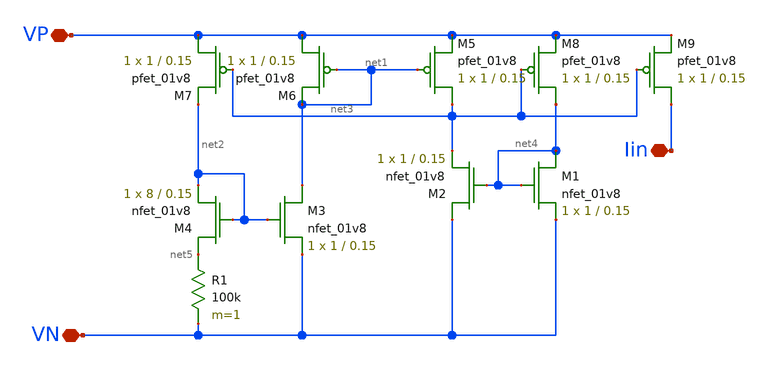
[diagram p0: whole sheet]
** sch_path: biasGen.sch
**.subckt biasGen VN Iin VP
*.iopin VN
*.iopin Iin
*.iopin VP
XM1 net4 net4 VN GND sky130_fd_pr__nfet_01v8 L=0.15 W=1 nf=1 ad='int((nf+1)/2) * W/nf * 0.29' as='int((nf+2)/2) * W/nf * 0.29'
+ pd='2*int((nf+1)/2) * (W/nf + 0.29)' ps='2*int((nf+2)/2) * (W/nf + 0.29)' nrd='0.29 / W' nrs='0.29 / W'
+ sa=0 sb=0 sd=0 mult=1 m=1
XM2 VN net4 net3 GND sky130_fd_pr__nfet_01v8 L=0.15 W=1 nf=1 ad='int((nf+1)/2) * W/nf * 0.29' as='int((nf+2)/2) * W/nf * 0.29'
+ pd='2*int((nf+1)/2) * (W/nf + 0.29)' ps='2*int((nf+2)/2) * (W/nf + 0.29)' nrd='0.29 / W' nrs='0.29 / W'
+ sa=0 sb=0 sd=0 mult=1 m=1
XM3 net1 net2 VN GND sky130_fd_pr__nfet_01v8 L=0.15 W=1 nf=1 ad='int((nf+1)/2) * W/nf * 0.29' as='int((nf+2)/2) * W/nf * 0.29'
+ pd='2*int((nf+1)/2) * (W/nf + 0.29)' ps='2*int((nf+2)/2) * (W/nf + 0.29)' nrd='0.29 / W' nrs='0.29 / W'
+ sa=0 sb=0 sd=0 mult=1 m=1
XM4 net5 net2 net2 GND sky130_fd_pr__nfet_01v8 L=0.15 W=8 nf=1 ad='int((nf+1)/2) * W/nf * 0.29' as='int((nf+2)/2) * W/nf * 0.29'
+ pd='2*int((nf+1)/2) * (W/nf + 0.29)' ps='2*int((nf+2)/2) * (W/nf + 0.29)' nrd='0.29 / W' nrs='0.29 / W'
+ sa=0 sb=0 sd=0 mult=1 m=1
XM5 net3 net1 VP VDD sky130_fd_pr__pfet_01v8 L=0.15 W=1 nf=1 ad='int((nf+1)/2) * W/nf * 0.29' as='int((nf+2)/2) * W/nf * 0.29'
+ pd='2*int((nf+1)/2) * (W/nf + 0.29)' ps='2*int((nf+2)/2) * (W/nf + 0.29)' nrd='0.29 / W' nrs='0.29 / W'
+ sa=0 sb=0 sd=0 mult=1 m=1
XM6 VP net1 net1 VDD sky130_fd_pr__pfet_01v8 L=0.15 W=1 nf=1 ad='int((nf+1)/2) * W/nf * 0.29' as='int((nf+2)/2) * W/nf * 0.29'
+ pd='2*int((nf+1)/2) * (W/nf + 0.29)' ps='2*int((nf+2)/2) * (W/nf + 0.29)' nrd='0.29 / W' nrs='0.29 / W'
+ sa=0 sb=0 sd=0 mult=1 m=1
XM7 VP net3 net2 VDD sky130_fd_pr__pfet_01v8 L=0.15 W=1 nf=1 ad='int((nf+1)/2) * W/nf * 0.29' as='int((nf+2)/2) * W/nf * 0.29'
+ pd='2*int((nf+1)/2) * (W/nf + 0.29)' ps='2*int((nf+2)/2) * (W/nf + 0.29)' nrd='0.29 / W' nrs='0.29 / W'
+ sa=0 sb=0 sd=0 mult=1 m=1
XM8 net4 net3 VP VDD sky130_fd_pr__pfet_01v8 L=0.15 W=1 nf=1 ad='int((nf+1)/2) * W/nf * 0.29' as='int((nf+2)/2) * W/nf * 0.29'
+ pd='2*int((nf+1)/2) * (W/nf + 0.29)' ps='2*int((nf+2)/2) * (W/nf + 0.29)' nrd='0.29 / W' nrs='0.29 / W'
+ sa=0 sb=0 sd=0 mult=1 m=1
R1 net5 VN 100k m=1
XM9 Iin net3 VP VDD sky130_fd_pr__pfet_01v8 L=0.15 W=1 nf=1 ad='int((nf+1)/2) * W/nf * 0.29' as='int((nf+2)/2) * W/nf * 0.29'
+ pd='2*int((nf+1)/2) * (W/nf + 0.29)' ps='2*int((nf+2)/2) * (W/nf + 0.29)' nrd='0.29 / W' nrs='0.29 / W'
+ sa=0 sb=0 sd=0 mult=1 m=1
**.ends
.end
